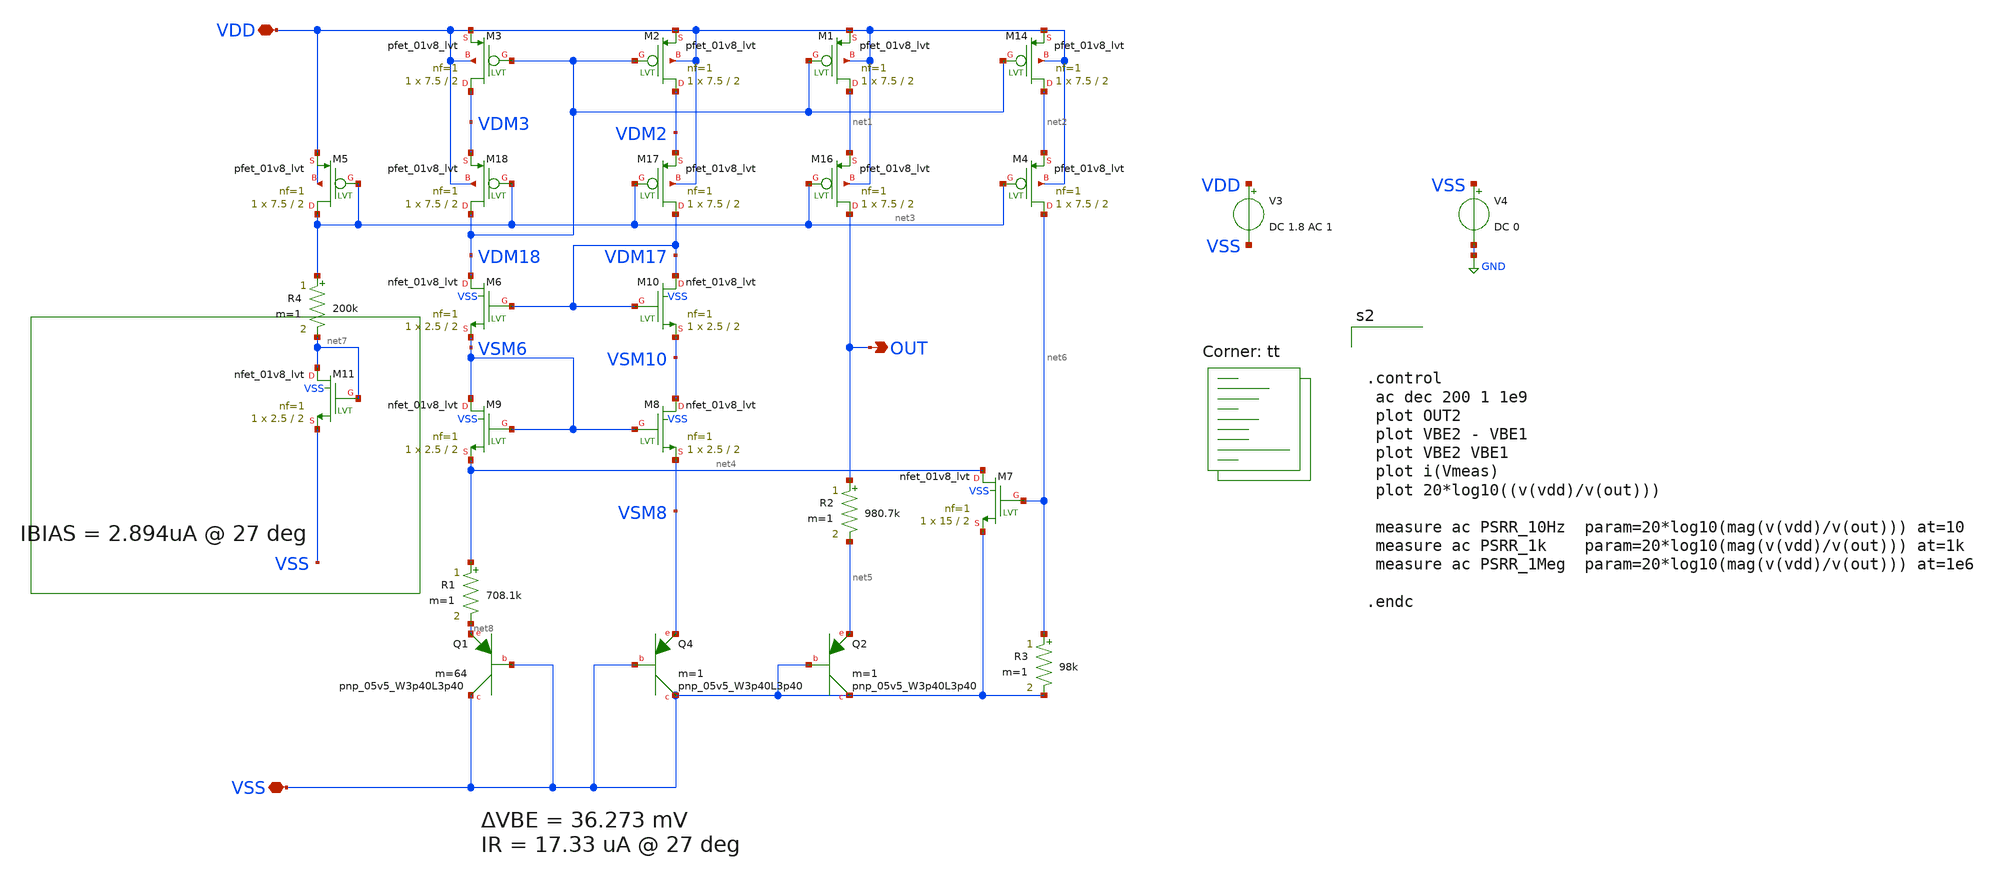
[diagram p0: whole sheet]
** sch_path: bandgap/tb_bgr1/tb_psrr.sch
**.subckt tb_psrr VDD VSS OUT
*.iopin VDD
*.iopin VSS
*.opin OUT
R1 net4 net8 708.1k m=1
R2 OUT net5 980.7k m=1
R3 net6 VSS 98k m=1
XQ4 VSS VSS VSM8 sky130_fd_pr__pnp_05v5_W3p40L3p40 m=1
XQ1 VSS VSS net8 sky130_fd_pr__pnp_05v5_W3p40L3p40 m=64
XQ2 VSS VSS net5 sky130_fd_pr__pnp_05v5_W3p40L3p40 m=1
XM14 net2 VDM18 VDD VDD sky130_fd_pr__pfet_01v8_lvt L=2 W=7.5 nf=1 ad='int((nf+1)/2) * W/nf * 0.29' as='int((nf+2)/2) * W/nf * 0.29'
+ pd='2*int((nf+1)/2) * (W/nf + 0.29)' ps='2*int((nf+2)/2) * (W/nf + 0.29)' nrd='0.29 / W' nrs='0.29 / W'
+ sa=0 sb=0 sd=0 mult=1 m=1
XM1 net1 VDM18 VDD VDD sky130_fd_pr__pfet_01v8_lvt L=2 W=7.5 nf=1 ad='int((nf+1)/2) * W/nf * 0.29' as='int((nf+2)/2) * W/nf * 0.29'
+ pd='2*int((nf+1)/2) * (W/nf + 0.29)' ps='2*int((nf+2)/2) * (W/nf + 0.29)' nrd='0.29 / W' nrs='0.29 / W'
+ sa=0 sb=0 sd=0 mult=1 m=1
XM2 VDM2 VDM18 VDD VDD sky130_fd_pr__pfet_01v8_lvt L=2 W=7.5 nf=1 ad='int((nf+1)/2) * W/nf * 0.29' as='int((nf+2)/2) * W/nf * 0.29'
+ pd='2*int((nf+1)/2) * (W/nf + 0.29)' ps='2*int((nf+2)/2) * (W/nf + 0.29)' nrd='0.29 / W' nrs='0.29 / W'
+ sa=0 sb=0 sd=0 mult=1 m=1
XM3 VDM3 VDM18 VDD VDD sky130_fd_pr__pfet_01v8_lvt L=2 W=7.5 nf=1 ad='int((nf+1)/2) * W/nf * 0.29' as='int((nf+2)/2) * W/nf * 0.29'
+ pd='2*int((nf+1)/2) * (W/nf + 0.29)' ps='2*int((nf+2)/2) * (W/nf + 0.29)' nrd='0.29 / W' nrs='0.29 / W'
+ sa=0 sb=0 sd=0 mult=1 m=1
XM4 net6 net3 net2 VDD sky130_fd_pr__pfet_01v8_lvt L=2 W=7.5 nf=1 ad='int((nf+1)/2) * W/nf * 0.29' as='int((nf+2)/2) * W/nf * 0.29'
+ pd='2*int((nf+1)/2) * (W/nf + 0.29)' ps='2*int((nf+2)/2) * (W/nf + 0.29)' nrd='0.29 / W' nrs='0.29 / W'
+ sa=0 sb=0 sd=0 mult=1 m=1
XM16 OUT net3 net1 VDD sky130_fd_pr__pfet_01v8_lvt L=2 W=7.5 nf=1 ad='int((nf+1)/2) * W/nf * 0.29' as='int((nf+2)/2) * W/nf * 0.29'
+ pd='2*int((nf+1)/2) * (W/nf + 0.29)' ps='2*int((nf+2)/2) * (W/nf + 0.29)' nrd='0.29 / W' nrs='0.29 / W'
+ sa=0 sb=0 sd=0 mult=1 m=1
XM17 VDM17 net3 VDM2 VDD sky130_fd_pr__pfet_01v8_lvt L=2 W=7.5 nf=1 ad='int((nf+1)/2) * W/nf * 0.29'
+ as='int((nf+2)/2) * W/nf * 0.29' pd='2*int((nf+1)/2) * (W/nf + 0.29)' ps='2*int((nf+2)/2) * (W/nf + 0.29)'
+ nrd='0.29 / W' nrs='0.29 / W' sa=0 sb=0 sd=0 mult=1 m=1
XM18 VDM18 net3 VDM3 VDD sky130_fd_pr__pfet_01v8_lvt L=2 W=7.5 nf=1 ad='int((nf+1)/2) * W/nf * 0.29'
+ as='int((nf+2)/2) * W/nf * 0.29' pd='2*int((nf+1)/2) * (W/nf + 0.29)' ps='2*int((nf+2)/2) * (W/nf + 0.29)'
+ nrd='0.29 / W' nrs='0.29 / W' sa=0 sb=0 sd=0 mult=1 m=1
XM5 net3 net3 VDD VDD sky130_fd_pr__pfet_01v8_lvt L=2 W=7.5 nf=1 ad='int((nf+1)/2) * W/nf * 0.29' as='int((nf+2)/2) * W/nf * 0.29'
+ pd='2*int((nf+1)/2) * (W/nf + 0.29)' ps='2*int((nf+2)/2) * (W/nf + 0.29)' nrd='0.29 / W' nrs='0.29 / W'
+ sa=0 sb=0 sd=0 mult=1 m=1
XM10 VDM17 VDM17 VSM10 VSS sky130_fd_pr__nfet_01v8_lvt L=2 W=2.5 nf=1 ad='int((nf+1)/2) * W/nf * 0.29'
+ as='int((nf+2)/2) * W/nf * 0.29' pd='2*int((nf+1)/2) * (W/nf + 0.29)' ps='2*int((nf+2)/2) * (W/nf + 0.29)'
+ nrd='0.29 / W' nrs='0.29 / W' sa=0 sb=0 sd=0 mult=1 m=1
XM6 VDM18 VDM17 VSM6 VSS sky130_fd_pr__nfet_01v8_lvt L=2 W=2.5 nf=1 ad='int((nf+1)/2) * W/nf * 0.29'
+ as='int((nf+2)/2) * W/nf * 0.29' pd='2*int((nf+1)/2) * (W/nf + 0.29)' ps='2*int((nf+2)/2) * (W/nf + 0.29)'
+ nrd='0.29 / W' nrs='0.29 / W' sa=0 sb=0 sd=0 mult=1 m=1
XM7 net4 net6 VSS VSS sky130_fd_pr__nfet_01v8_lvt L=2 W=15 nf=1 ad='int((nf+1)/2) * W/nf * 0.29' as='int((nf+2)/2) * W/nf * 0.29'
+ pd='2*int((nf+1)/2) * (W/nf + 0.29)' ps='2*int((nf+2)/2) * (W/nf + 0.29)' nrd='0.29 / W' nrs='0.29 / W'
+ sa=0 sb=0 sd=0 mult=1 m=1
XM8 VSM10 VSM6 VSM8 VSS sky130_fd_pr__nfet_01v8_lvt L=2 W=2.5 nf=1 ad='int((nf+1)/2) * W/nf * 0.29' as='int((nf+2)/2) * W/nf * 0.29'
+ pd='2*int((nf+1)/2) * (W/nf + 0.29)' ps='2*int((nf+2)/2) * (W/nf + 0.29)' nrd='0.29 / W' nrs='0.29 / W'
+ sa=0 sb=0 sd=0 mult=1 m=1
XM9 VSM6 VSM6 net4 VSS sky130_fd_pr__nfet_01v8_lvt L=2 W=2.5 nf=1 ad='int((nf+1)/2) * W/nf * 0.29' as='int((nf+2)/2) * W/nf * 0.29'
+ pd='2*int((nf+1)/2) * (W/nf + 0.29)' ps='2*int((nf+2)/2) * (W/nf + 0.29)' nrd='0.29 / W' nrs='0.29 / W'
+ sa=0 sb=0 sd=0 mult=1 m=1
R4 net3 net7 200k m=1
XM11 net7 net7 VSS VSS sky130_fd_pr__nfet_01v8_lvt L=2 W=2.5 nf=1 ad='int((nf+1)/2) * W/nf * 0.29' as='int((nf+2)/2) * W/nf * 0.29'
+ pd='2*int((nf+1)/2) * (W/nf + 0.29)' ps='2*int((nf+2)/2) * (W/nf + 0.29)' nrd='0.29 / W' nrs='0.29 / W'
+ sa=0 sb=0 sd=0 mult=1 m=1
V3 VDD VSS DC 1.8 AC 1
V4 VSS GND DC 0
**** begin user architecture code
.lib $::SKYWATER_MODELS/sky130.lib.spice tt



.control
 ac dec 200 1 1e9
 plot OUT2
 plot VBE2 - VBE1
 plot VBE2 VBE1
 plot i(Vmeas)
 plot 20*log10((v(vdd)/v(out)))

 measure ac PSRR_10Hz  param=20*log10(mag(v(vdd)/v(out))) at=10
 measure ac PSRR_1k    param=20*log10(mag(v(vdd)/v(out))) at=1k
 measure ac PSRR_1Meg  param=20*log10(mag(v(vdd)/v(out))) at=1e6

.endc


**** end user architecture code
**.ends
.GLOBAL GND
.end
